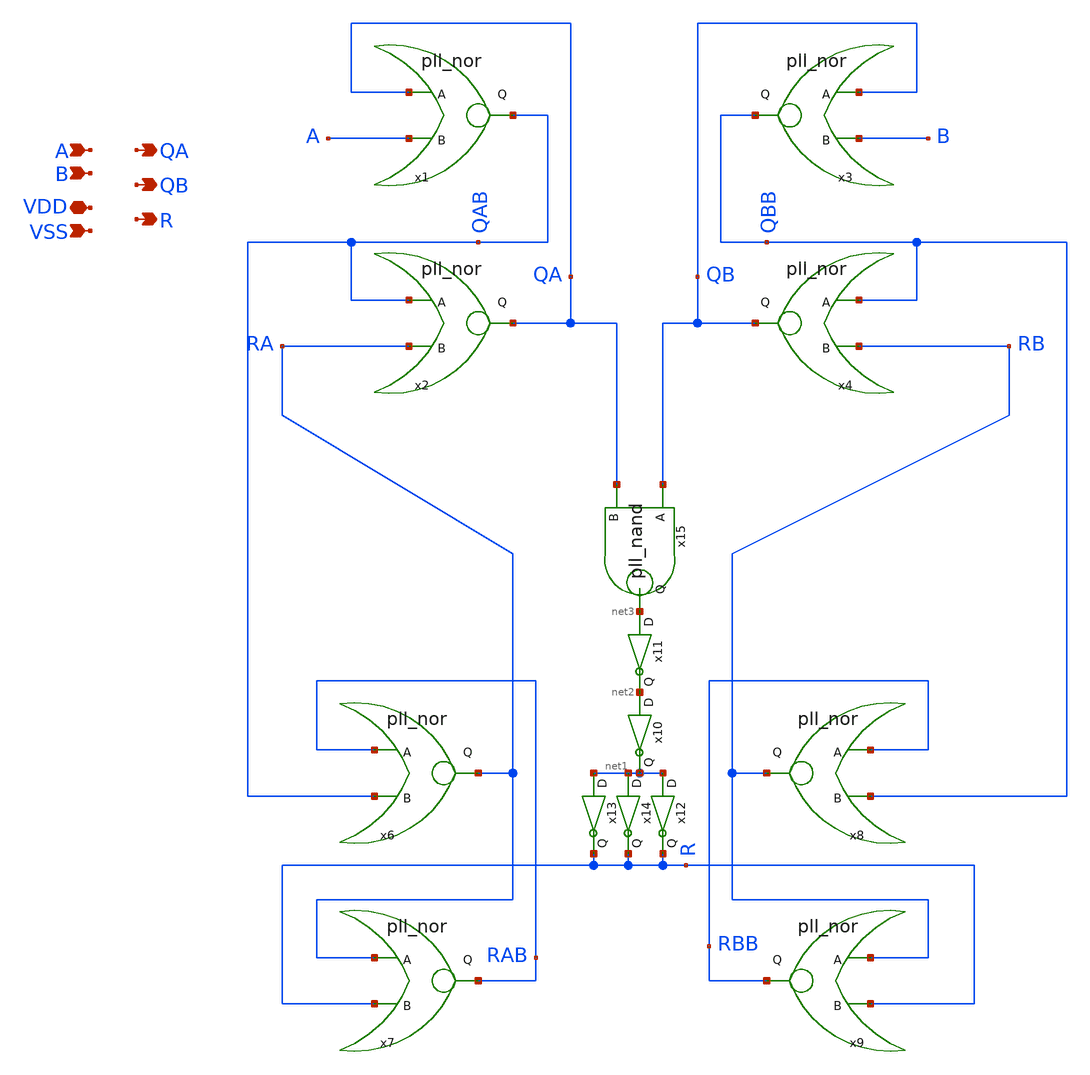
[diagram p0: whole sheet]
** sch_path: xschem/pll_pfd.sch
**.subckt pll_pfd A B VDD VSS QA QB R
*.ipin A
*.ipin B
*.iopin VDD
*.ipin VSS
*.opin QA
*.opin QB
*.opin R
x1 QA A QAB VDD VSS pll_nor
x2 QAB RA QA VDD VSS pll_nor
x3 QB B QBB VDD VSS pll_nor
x4 QBB RB QB VDD VSS pll_nor
x6 RAB QAB RA VDD VSS pll_nor
x7 RA R RAB VDD VSS pll_nor
x8 RBB QBB RB VDD VSS pll_nor
x9 RB R RBB VDD VSS pll_nor
x10 net2 net1 VDD VSS pll_inv1
x11 net3 net2 VDD VSS pll_inv1
x12 net1 R VDD VSS pll_inv1
x13 net1 R VDD VSS pll_inv1
x14 net1 R VDD VSS pll_inv1
x15 QB QA net3 VDD VSS pll_nand
**.ends
.end
